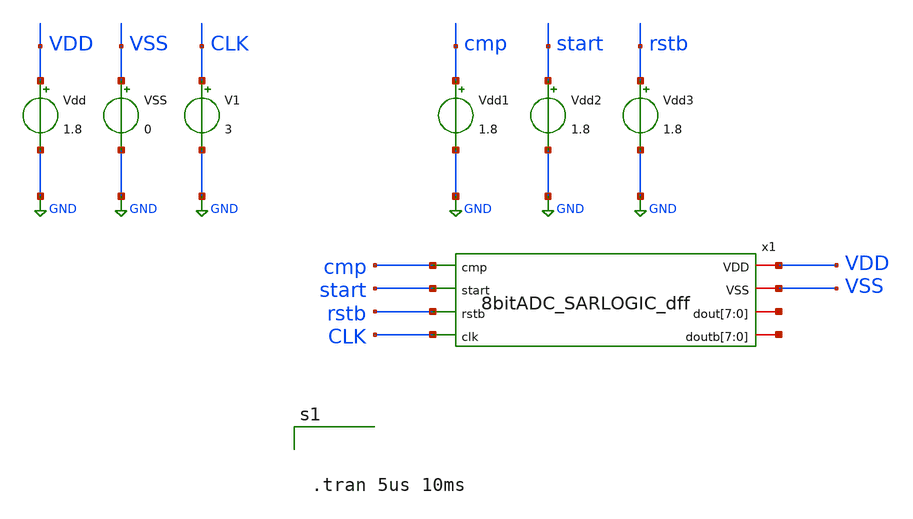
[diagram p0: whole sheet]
** sch_path: 8bitADC_SARLOGIC_tb.sch
**.subckt 8bitADC_SARLOGIC_tb
Vdd VDD GND 1.8
VSS VSS GND 0
Vdd1 cmp GND 1.8
Vdd2 start GND 1.8
Vdd3 rstb GND 1.8
x1 VDD cmp start VSS net1[7] net1[6] net1[5] net1[4] net1[3] net1[2] net1[1] net1[0] rstb net2[7]
+ net2[6] net2[5] net2[4] net2[3] net2[2] net2[1] net2[0] CLK 8bitADC_SARLOGIC_dff
V1 CLK GND 3
**** begin user architecture code

** opencircuitdesign pdks install
.lib $::SKYWATER_MODELS/sky130.lib.spice tt
.include $::SKYWATER_STDCELLS/sky130_fd_sc_hd.spice





.tran 5us 10ms



**** end user architecture code
**.ends

* expanding   symbol:  8bitADC_SARLOGIC_dff.sym # of pins=8
** sym_path: 8bitADC_SARLOGIC_dff.sym
** sch_path: 8bitADC_SARLOGIC_dff.sch
.subckt 8bitADC_SARLOGIC_dff VDD cmp start VSS dout[7] dout[6] dout[5] dout[4] dout[3] dout[2]
+ dout[1] dout[0] rstb doutb[7] doutb[6] doutb[5] doutb[4] doutb[3] doutb[2] doutb[1] doutb[0] clk
*.ipin cmp
*.ipin start
*.ipin rstb
*.ipin clk
*.iopin dout[7],dout[6],dout[5],dout[4],dout[3],dout[2],dout[1],dout[0]
*.iopin doutb[7],doutb[6],doutb[5],doutb[4],doutb[3],doutb[2],doutb[1],doutb[0]
*.iopin VSS
*.iopin VDD
x18 cmp VSS VNB VPB VDD net3 sky130_fd_sc_hd__buf_1
x19 clk VSS VNB VPB VDD clk_t sky130_fd_sc_hd__buf_1
x20 net1 VSS VNB VPB VDD net2 sky130_fd_sc_hd__buf_1
x21 rstb VSS VNB VPB VDD net1 sky130_fd_sc_hd__buf_1
x22 start VSS VNB VPB VDD net12 sky130_fd_sc_hd__buf_1
x23 dout[6] net3 net2 net4 VSS VNB VPB VDD dout[7] doutb[7] sky130_fd_sc_hd__dfbbp_1
x1 dout[5] net3 net2 net6 VSS VNB VPB VDD dout[6] doutb[6] sky130_fd_sc_hd__dfbbp_1
x3 dout[4] net3 net2 net7 VSS VNB VPB VDD dout[5] doutb[5] sky130_fd_sc_hd__dfbbp_1
x4 dout[3] net3 net2 net8 VSS VNB VPB VDD dout[4] doutb[4] sky130_fd_sc_hd__dfbbp_1
x5 dout[2] net3 net2 net5 VSS VNB VPB VDD dout[3] doutb[3] sky130_fd_sc_hd__dfbbp_1
x6 dout[1] net3 net2 net9 VSS VNB VPB VDD dout[2] doutb[2] sky130_fd_sc_hd__dfbbp_1
x7 dout[0] net3 net2 net10 VSS VNB VPB VDD dout[1] doutb[1] sky130_fd_sc_hd__dfbbp_1
x8 net21 net3 net2 net11 VSS VNB VPB VDD dout[0] doutb[0] sky130_fd_sc_hd__dfbbp_1
x16 clk_t net12 net2 VSS VNB VPB VDD net14 net4 sky130_fd_sc_hd__dfrbp_1
x2 clk_t net14 net2 VSS VNB VPB VDD net13 net6 sky130_fd_sc_hd__dfrbp_1
x9 clk_t net13 net2 VSS VNB VPB VDD net15 net7 sky130_fd_sc_hd__dfrbp_1
x17 clk_t net15 net2 VSS VNB VPB VDD net16 net8 sky130_fd_sc_hd__dfrbp_1
x10 clk_t net16 net2 VSS VNB VPB VDD net17 net5 sky130_fd_sc_hd__dfrbp_1
x11 clk_t net17 net2 VSS VNB VPB VDD net18 net9 sky130_fd_sc_hd__dfrbp_1
x24 clk_t net18 net2 VSS VNB VPB VDD net19 net10 sky130_fd_sc_hd__dfrbp_1
x25 clk_t net19 net2 VSS VNB VPB VDD net20 net11 sky130_fd_sc_hd__dfrbp_1
x12 clk_t net20 net2 VSS VNB VPB VDD net21 net22 sky130_fd_sc_hd__dfrbp_1
**** begin user architecture code



.tran 5us 10ms



**** end user architecture code
.ends

.GLOBAL GND
.end
